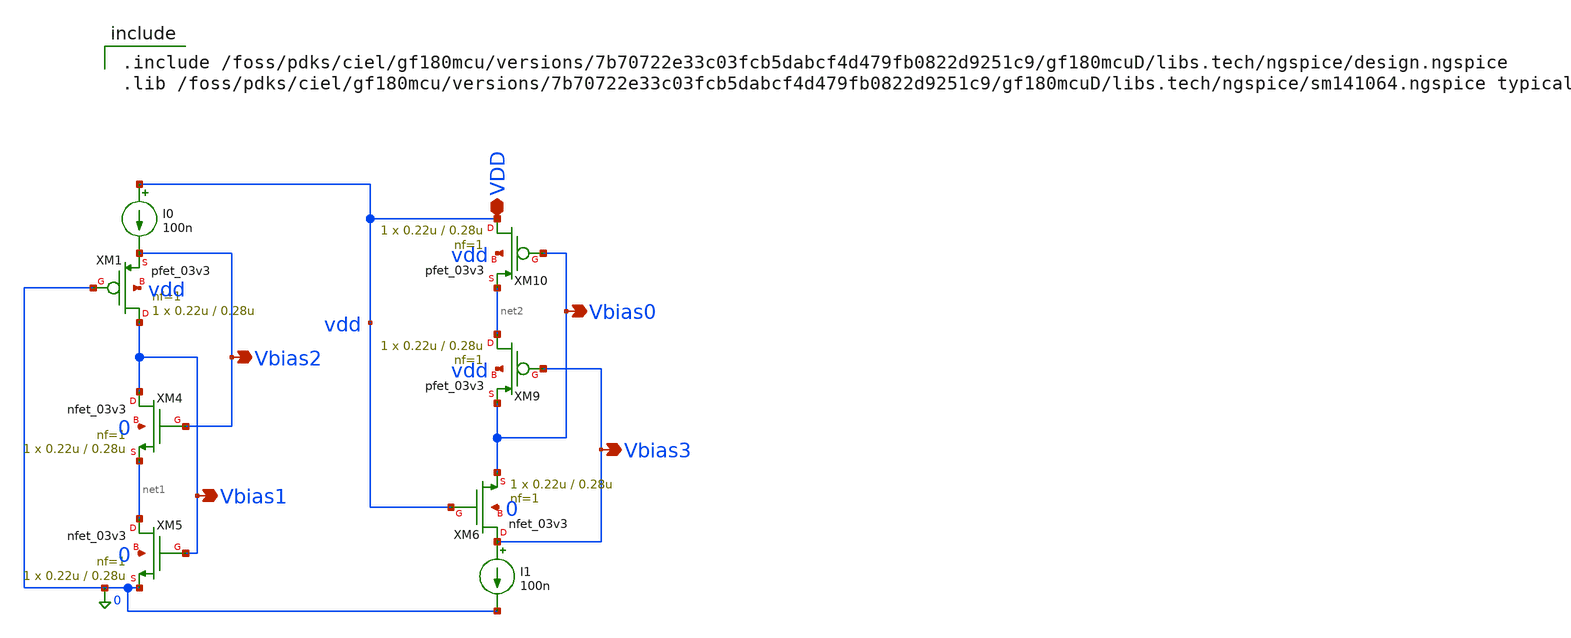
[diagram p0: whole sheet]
** sch_path: analog/B04_OTA_test_bias.sch
**.subckt B04_OTA_test_bias VDD Vbias2 Vbias1 Vbias0 Vbias3
*.iopin VDD
*.opin Vbias2
*.opin Vbias1
*.opin Vbias0
*.opin Vbias3
XM1 Vbias1 0 Vbias2 vdd pfet_03v3 L=0.28u W=0.22u nf=1 ad='int((nf+1)/2) * W/nf * 0.18u' as='int((nf+2)/2) * W/nf * 0.18u'
+ pd='2*int((nf+1)/2) * (W/nf + 0.18u)' ps='2*int((nf+2)/2) * (W/nf + 0.18u)' nrd='0.18u / W' nrs='0.18u / W'
+ sa=0 sb=0 sd=0 m=1
XM4 Vbias1 Vbias2 net1 0 nfet_03v3 L=0.28u W=0.22u nf=1 ad='int((nf+1)/2) * W/nf * 0.18u' as='int((nf+2)/2) * W/nf * 0.18u'
+ pd='2*int((nf+1)/2) * (W/nf + 0.18u)' ps='2*int((nf+2)/2) * (W/nf + 0.18u)' nrd='0.18u / W' nrs='0.18u / W'
+ sa=0 sb=0 sd=0 m=1
XM5 net1 Vbias1 0 0 nfet_03v3 L=0.28u W=0.22u nf=1 ad='int((nf+1)/2) * W/nf * 0.18u' as='int((nf+2)/2) * W/nf * 0.18u'
+ pd='2*int((nf+1)/2) * (W/nf + 0.18u)' ps='2*int((nf+2)/2) * (W/nf + 0.18u)' nrd='0.18u / W' nrs='0.18u / W'
+ sa=0 sb=0 sd=0 m=1
XM9 net2 Vbias3 Vbias0 vdd pfet_03v3 L=0.28u W=0.22u nf=1 ad='int((nf+1)/2) * W/nf * 0.18u' as='int((nf+2)/2) * W/nf * 0.18u'
+ pd='2*int((nf+1)/2) * (W/nf + 0.18u)' ps='2*int((nf+2)/2) * (W/nf + 0.18u)' nrd='0.18u / W' nrs='0.18u / W'
+ sa=0 sb=0 sd=0 m=1
XM10 vdd Vbias0 net2 vdd pfet_03v3 L=0.28u W=0.22u nf=1 ad='int((nf+1)/2) * W/nf * 0.18u' as='int((nf+2)/2) * W/nf * 0.18u'
+ pd='2*int((nf+1)/2) * (W/nf + 0.18u)' ps='2*int((nf+2)/2) * (W/nf + 0.18u)' nrd='0.18u / W' nrs='0.18u / W'
+ sa=0 sb=0 sd=0 m=1
XM6 Vbias3 vdd Vbias0 0 nfet_03v3 L=0.28u W=0.22u nf=1 ad='int((nf+1)/2) * W/nf * 0.18u' as='int((nf+2)/2) * W/nf * 0.18u'
+ pd='2*int((nf+1)/2) * (W/nf + 0.18u)' ps='2*int((nf+2)/2) * (W/nf + 0.18u)' nrd='0.18u / W' nrs='0.18u / W'
+ sa=0 sb=0 sd=0 m=1
I0 vdd Vbias2 100n
I1 Vbias3 0 100n
**** begin user architecture code

.include /foss/pdks/ciel/gf180mcu/versions/7b70722e33c03fcb5dabcf4d479fb0822d9251c9/gf180mcuD/libs.tech/ngspice/design.ngspice
.lib /foss/pdks/ciel/gf180mcu/versions/7b70722e33c03fcb5dabcf4d479fb0822d9251c9/gf180mcuD/libs.tech/ngspice/sm141064.ngspice typical

**** end user architecture code
**.ends
.end
